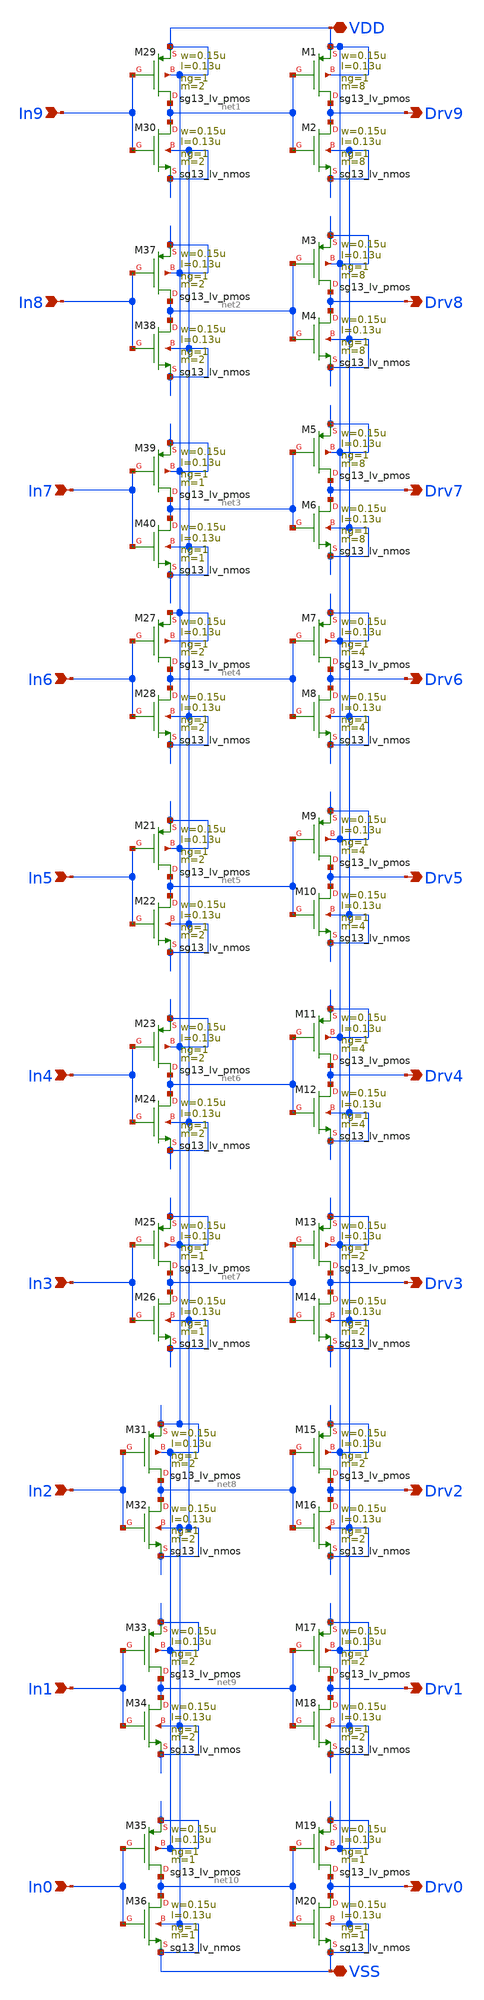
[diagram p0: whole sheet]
** sch_path: circuit_files/xschem_symbols/capDrivers.sch
**.subckt capDrivers VDD VSS Drv9 Drv8 Drv7 Drv6 Drv5 Drv4 Drv3 Drv2 Drv1 Drv0 In9 In8 In7 In6 In5
*+ In4 In3 In2 In1 In0
*.iopin VDD
*.iopin VSS
*.opin Drv9
*.opin Drv8
*.opin Drv7
*.opin Drv6
*.opin Drv5
*.opin Drv4
*.opin Drv3
*.opin Drv2
*.opin Drv1
*.opin Drv0
*.ipin In9
*.ipin In8
*.ipin In7
*.ipin In6
*.ipin In5
*.ipin In4
*.ipin In3
*.ipin In2
*.ipin In1
*.ipin In0
XM1 Drv9 net1 VDD VDD sg13_lv_pmos w=0.15u l=0.13u ng=1 m=8 mm_ok=1
XM2 Drv9 net1 VSS VSS sg13_lv_nmos w=0.15u l=0.13u ng=1 m=8 mm_ok=1
XM3 Drv8 net2 VDD VDD sg13_lv_pmos w=0.15u l=0.13u ng=1 m=8 mm_ok=1
XM4 Drv8 net2 VSS VSS sg13_lv_nmos w=0.15u l=0.13u ng=1 m=8 mm_ok=1
XM5 Drv7 net3 VDD VDD sg13_lv_pmos w=0.15u l=0.13u ng=1 m=8 mm_ok=1
XM6 Drv7 net3 VSS VSS sg13_lv_nmos w=0.15u l=0.13u ng=1 m=8 mm_ok=1
XM7 Drv6 net4 VDD VDD sg13_lv_pmos w=0.15u l=0.13u ng=1 m=4 mm_ok=1
XM8 Drv6 net4 VSS VSS sg13_lv_nmos w=0.15u l=0.13u ng=1 m=4 mm_ok=1
XM9 Drv5 net5 VDD VDD sg13_lv_pmos w=0.15u l=0.13u ng=1 m=4 mm_ok=1
XM10 Drv5 net5 VSS VSS sg13_lv_nmos w=0.15u l=0.13u ng=1 m=4 mm_ok=1
XM11 Drv4 net6 VDD VDD sg13_lv_pmos w=0.15u l=0.13u ng=1 m=4 mm_ok=1
XM12 Drv4 net6 VSS VSS sg13_lv_nmos w=0.15u l=0.13u ng=1 m=4 mm_ok=1
XM13 Drv3 net7 VDD VDD sg13_lv_pmos w=0.15u l=0.13u ng=1 m=2 mm_ok=1
XM14 Drv3 net7 VSS VSS sg13_lv_nmos w=0.15u l=0.13u ng=1 m=2 mm_ok=1
XM15 Drv2 net8 VDD VDD sg13_lv_pmos w=0.15u l=0.13u ng=1 m=2 mm_ok=1
XM16 Drv2 net8 VSS VSS sg13_lv_nmos w=0.15u l=0.13u ng=1 m=2 mm_ok=1
XM17 Drv1 net9 VDD VDD sg13_lv_pmos w=0.15u l=0.13u ng=1 m=2 mm_ok=1
XM18 Drv1 net9 VSS VSS sg13_lv_nmos w=0.15u l=0.13u ng=1 m=2 mm_ok=1
XM19 Drv0 net10 VDD VDD sg13_lv_pmos w=0.15u l=0.13u ng=1 m=1 mm_ok=1
XM20 Drv0 net10 VSS VSS sg13_lv_nmos w=0.15u l=0.13u ng=1 m=1 mm_ok=1
XM31 net8 In2 VDD VDD sg13_lv_pmos w=0.15u l=0.13u ng=1 m=2 mm_ok=1
XM32 net8 In2 VSS VSS sg13_lv_nmos w=0.15u l=0.13u ng=1 m=2 mm_ok=1
XM33 net9 In1 VDD VDD sg13_lv_pmos w=0.15u l=0.13u ng=1 m=2 mm_ok=1
XM34 net9 In1 VSS VSS sg13_lv_nmos w=0.15u l=0.13u ng=1 m=2 mm_ok=1
XM35 net10 In0 VDD VDD sg13_lv_pmos w=0.15u l=0.13u ng=1 m=1 mm_ok=1
XM36 net10 In0 VSS VSS sg13_lv_nmos w=0.15u l=0.13u ng=1 m=1 mm_ok=1
XM21 net5 In5 VDD VDD sg13_lv_pmos w=0.15u l=0.13u ng=1 m=2 mm_ok=1
XM22 net5 In5 VSS VSS sg13_lv_nmos w=0.15u l=0.13u ng=1 m=2 mm_ok=1
XM23 net6 In4 VDD VDD sg13_lv_pmos w=0.15u l=0.13u ng=1 m=2 mm_ok=1
XM24 net6 In4 VSS VSS sg13_lv_nmos w=0.15u l=0.13u ng=1 m=2 mm_ok=1
XM25 net7 In3 VDD VDD sg13_lv_pmos w=0.15u l=0.13u ng=1 m=1 mm_ok=1
XM26 net7 In3 VSS VSS sg13_lv_nmos w=0.15u l=0.13u ng=1 m=1 mm_ok=1
XM27 net4 In6 VDD VDD sg13_lv_pmos w=0.15u l=0.13u ng=1 m=2 mm_ok=1
XM28 net4 In6 VSS VSS sg13_lv_nmos w=0.15u l=0.13u ng=1 m=2 mm_ok=1
XM29 net1 In9 VDD VDD sg13_lv_pmos w=0.15u l=0.13u ng=1 m=2 mm_ok=1
XM30 net1 In9 VSS VSS sg13_lv_nmos w=0.15u l=0.13u ng=1 m=2 mm_ok=1
XM37 net2 In8 VDD VDD sg13_lv_pmos w=0.15u l=0.13u ng=1 m=2 mm_ok=1
XM38 net2 In8 VSS VSS sg13_lv_nmos w=0.15u l=0.13u ng=1 m=2 mm_ok=1
XM39 net3 In7 VDD VDD sg13_lv_pmos w=0.15u l=0.13u ng=1 m=1 mm_ok=1
XM40 net3 In7 VSS VSS sg13_lv_nmos w=0.15u l=0.13u ng=1 m=1 mm_ok=1
**.ends
.end
